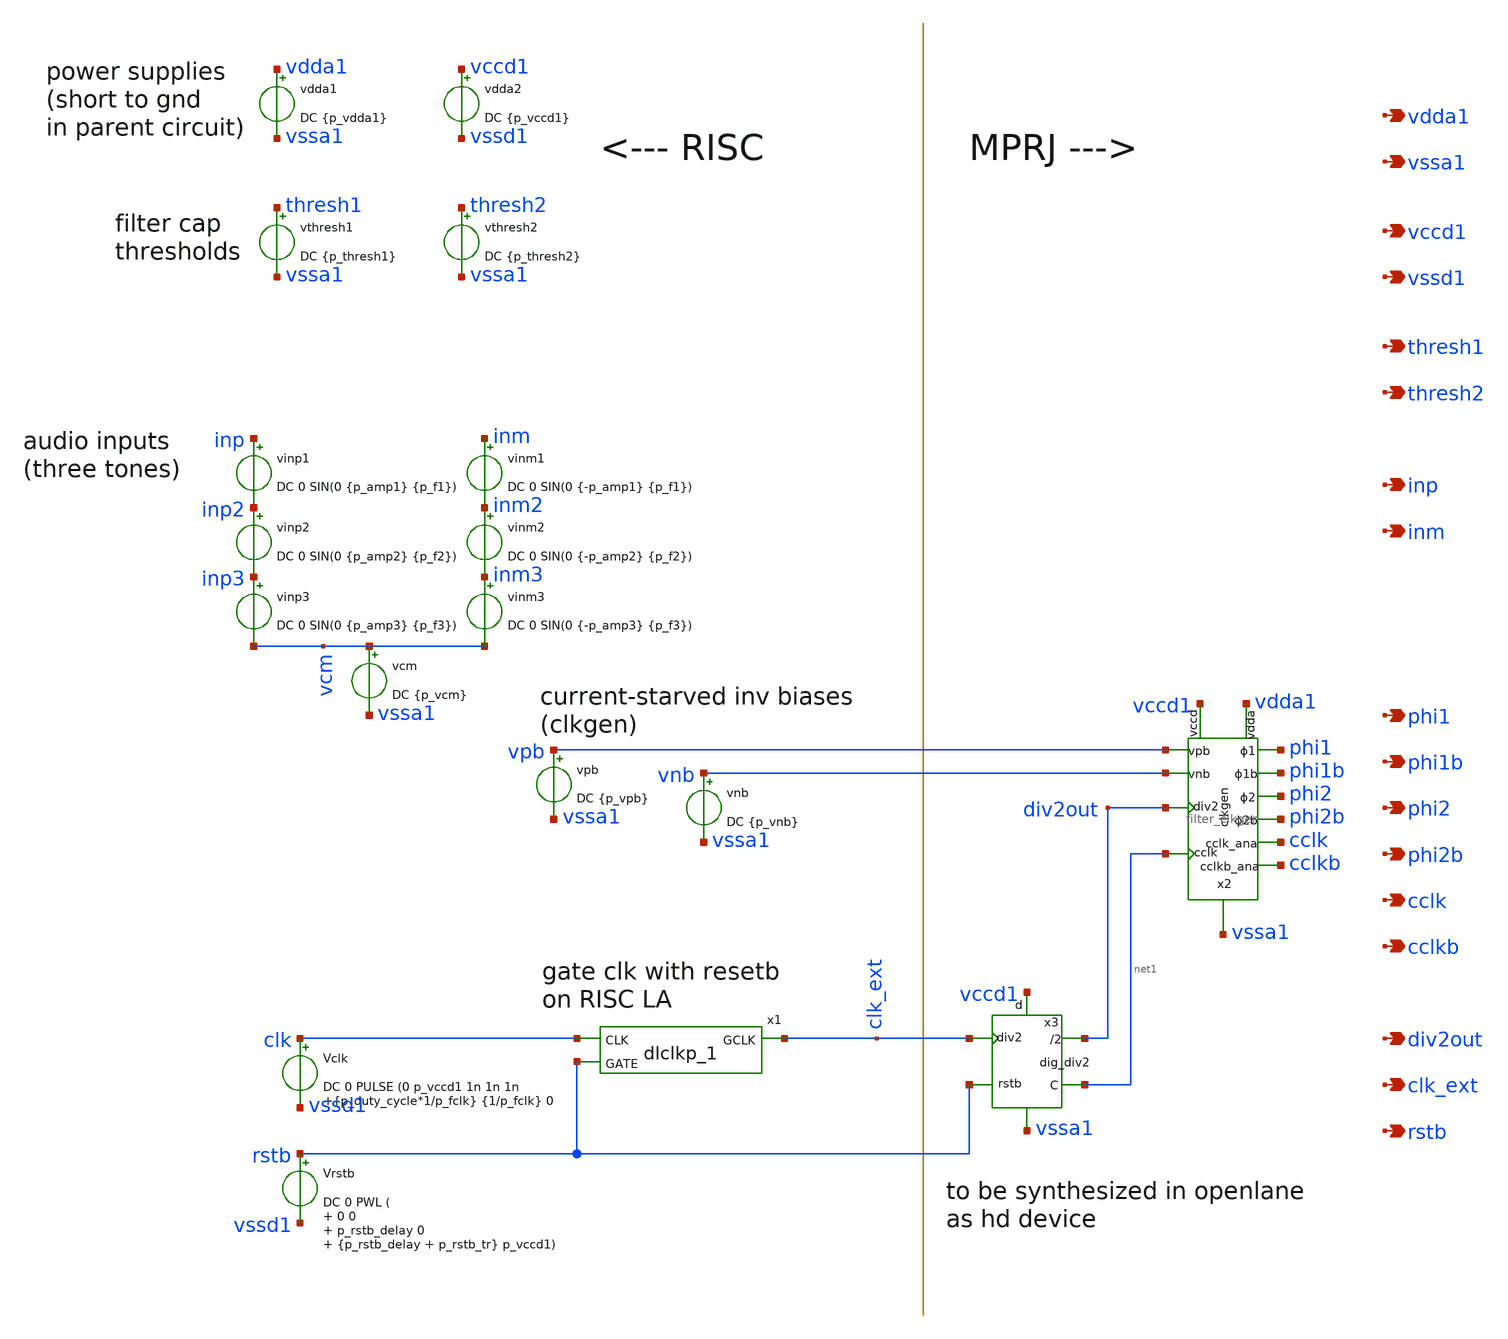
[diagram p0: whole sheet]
** sch_path: xschem/risc_signals.sch
**.subckt risc_signals thresh1 thresh2 vdda1 vssa1 inp inm phi1 phi1b vccd1 vssd1 div2out rstb phi2
*+ phi2b cclk cclkb clk_ext
*.opin thresh1
*.opin thresh2
*.opin vdda1
*.opin vssa1
*.opin inp
*.opin inm
*.opin phi1
*.opin phi1b
*.opin vccd1
*.opin vssd1
*.opin div2out
*.opin rstb
*.opin phi2
*.opin phi2b
*.opin cclk
*.opin cclkb
*.opin clk_ext
vdda1 vdda1 vssa1 DC {p_vdda1}
vthresh1 thresh1 vssa1 DC {p_thresh1}
vthresh2 thresh2 vssa1 DC {p_thresh2}
vinp1 inp inp2 DC 0 SIN(0 {p_amp1} {p_f1})
vinm1 inm inm2 DC 0 SIN(0 {-p_amp1} {p_f1})
vpb vpb vssa1 DC {p_vpb}
vnb vnb vssa1 DC {p_vnb}
vinp2 inp2 inp3 DC 0 SIN(0 {p_amp2} {p_f2})
vinp3 inp3 vcm DC 0 SIN(0 {p_amp3} {p_f3})
vinm2 inm2 inm3 DC 0 SIN(0 {-p_amp2} {p_f2})
vinm3 inm3 vcm DC 0 SIN(0 {-p_amp3} {p_f3})
vcm vcm vssa1 DC {p_vcm}
vdda2 vccd1 vssd1 DC {p_vccd1}
Vclk clk vssd1 DC 0 PULSE (0 p_vccd1 1n 1n 1n {p_duty_cycle*1/p_fclk} {1/p_fclk} 0
Vrstb rstb vssd1 DC 0 PWL ( 0 0 p_rstb_delay 0 {p_rstb_delay + p_rstb_tr} p_vccd1)
x1 clk rstb vssd1 vssd1 vccd1 vccd1 clk_ext sky130_fd_sc_hd__dlclkp_1
x2 net1 phi2b phi2 phi1b phi1 cclkb cclk vpb vnb vdda1 vssa1 vccd1 div2out filter_clkgen
x3 rstb net1 div2out vccd1 vssa1 clk_ext dig_div2
**.ends
.end
